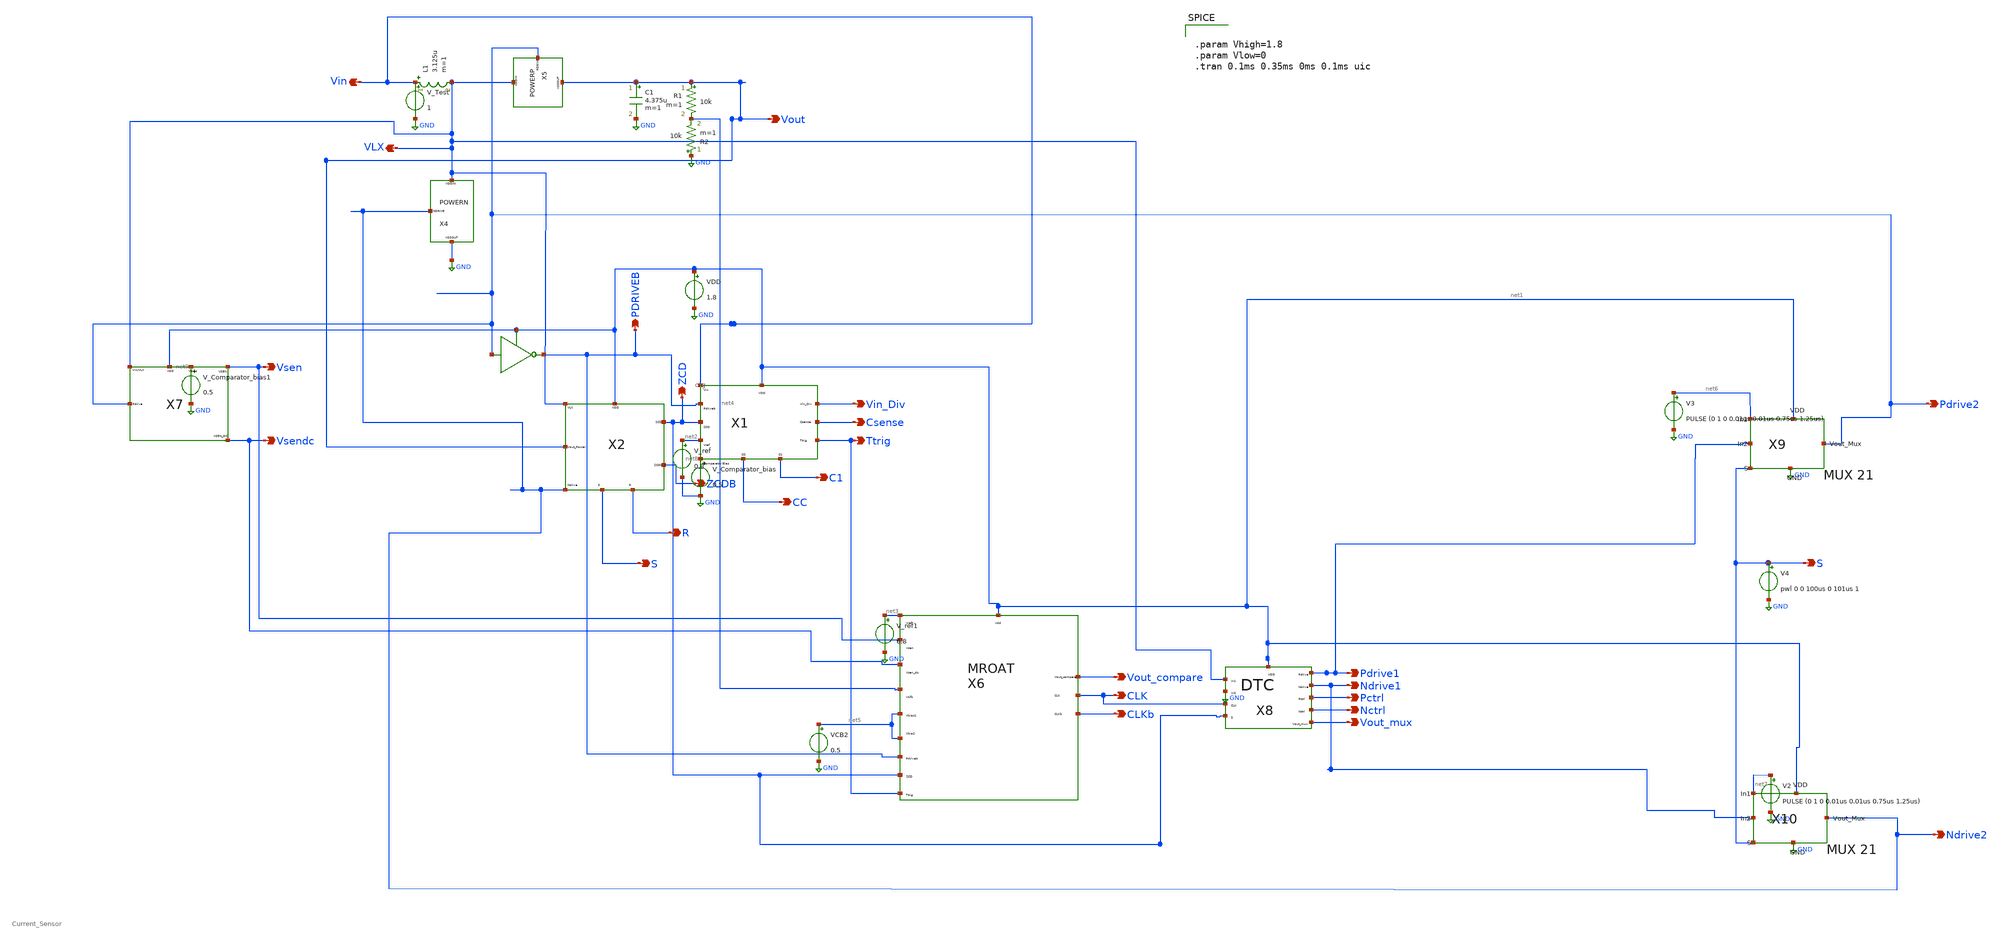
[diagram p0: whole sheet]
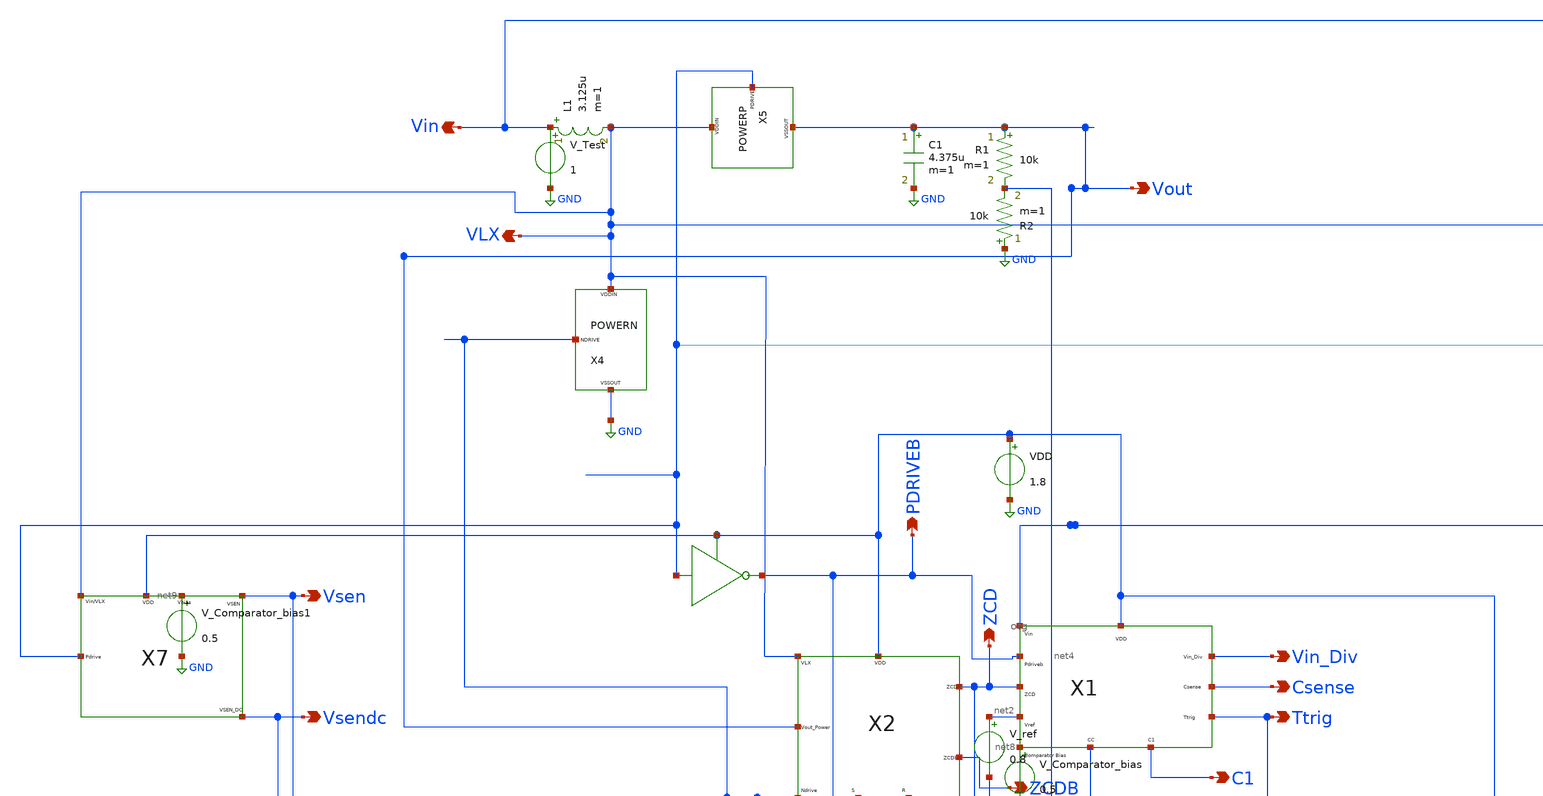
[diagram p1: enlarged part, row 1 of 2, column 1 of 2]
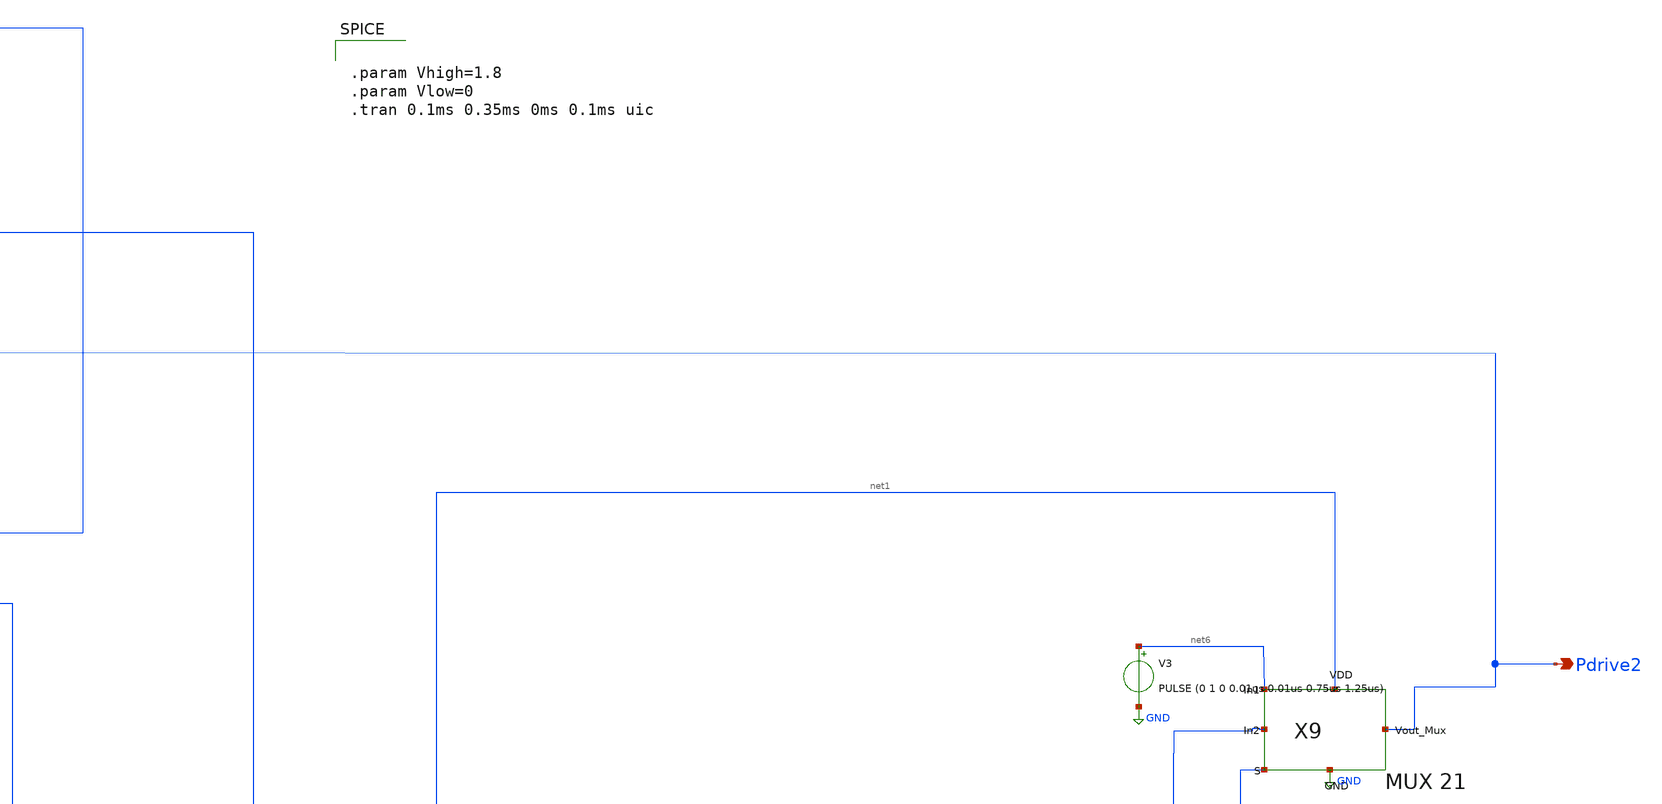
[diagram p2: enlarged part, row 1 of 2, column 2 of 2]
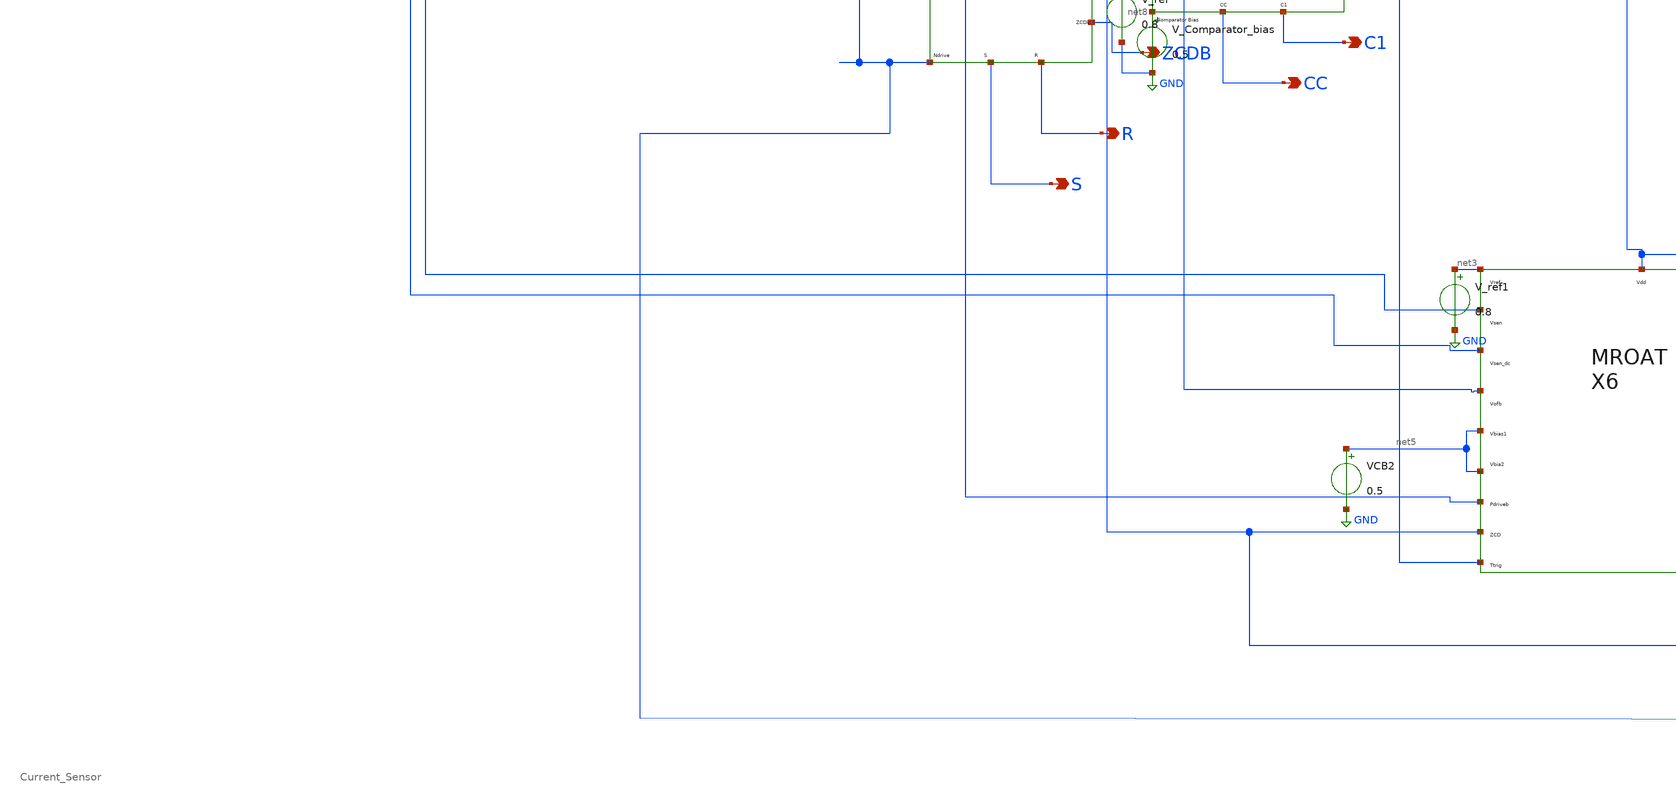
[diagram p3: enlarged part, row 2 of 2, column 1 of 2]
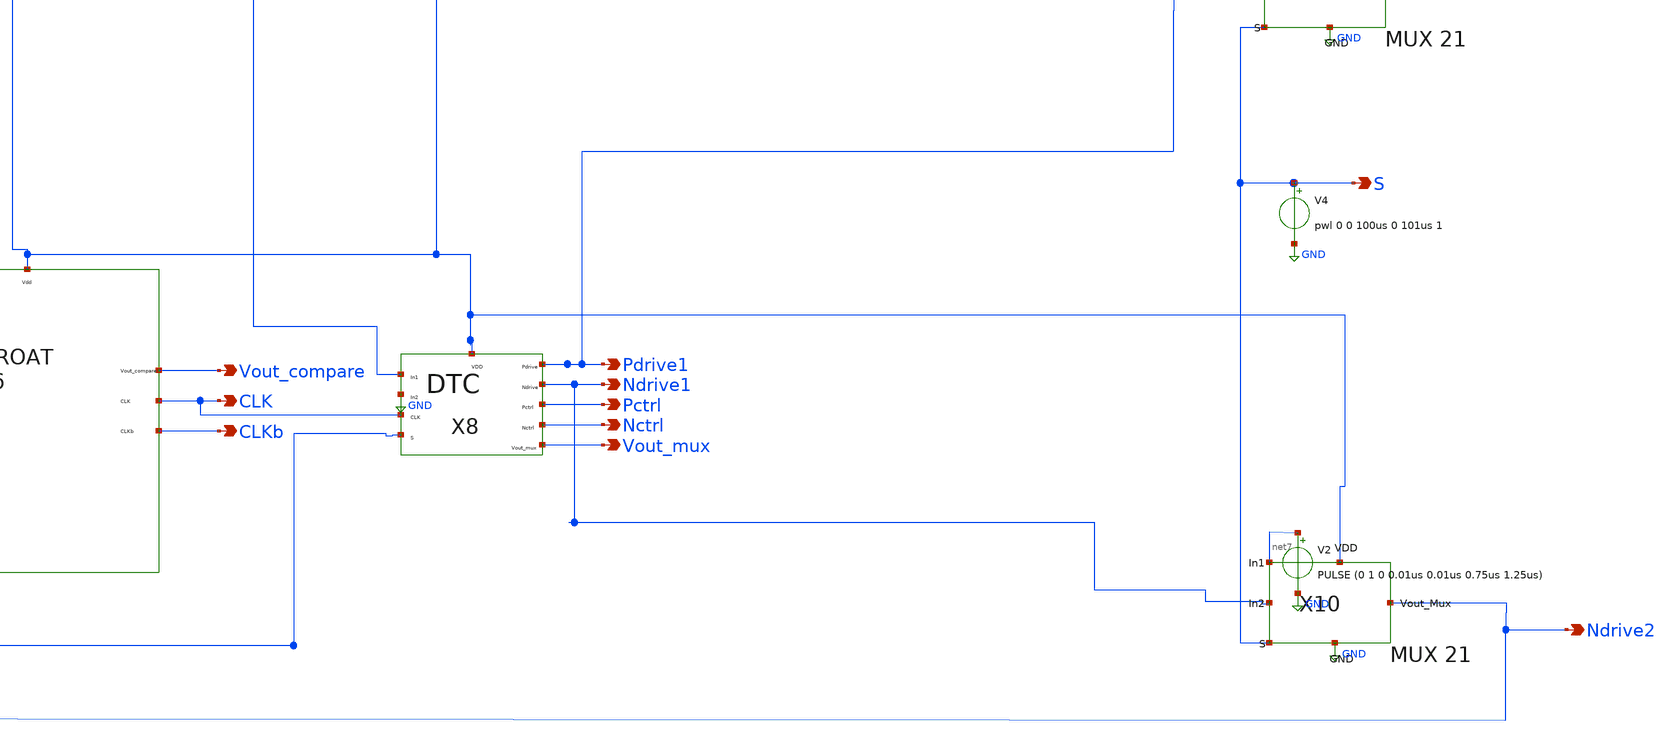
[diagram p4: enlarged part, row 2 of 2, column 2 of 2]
** sch_path: Current Sensor/fb_test.sch
**.subckt fb_test ZCD Vin_Div Csense Ttrig ZCDB PDRIVEB Vin VLX Vout C1 CC S R Vsen Vsendc
*+ Vout_compare CLK CLKb Pdrive1 Ndrive1 Pctrl Nctrl Vout_mux Pdrive2 Ndrive2 S
*.opin ZCD
*.opin Vin_Div
*.opin Csense
*.opin Ttrig
*.opin ZCDB
*.opin PDRIVEB
*.opin Vin
*.opin VLX
*.opin Vout
*.opin C1
*.opin CC
*.opin S
*.opin R
*.opin Vsen
*.opin Vsendc
*.opin Vout_compare
*.opin CLK
*.opin CLKb
*.opin Pdrive1
*.opin Ndrive1
*.opin Pctrl
*.opin Nctrl
*.opin Vout_mux
*.opin Pdrive2
*.opin Ndrive2
*.opin S
X1 Vin PDRIVEB ZCD net2 net8 net1 Vin_Div Csense Ttrig CC C1 otg
X2 VLX Vout Ndrive2 net1 ZCD ZCDB S R zcd
VDD net1 GND 1.8
V_Comparator_bias net8 GND 0.5
V_ref net2 GND 0.8
C1 Vout GND 4.375u m=1
R1 Vout net4 10k m=1
L1 Vin VLX 3.125u m=1
X4 Ndrive2 VLX GND powern
X5 Pdrive2 VLX Vout powerp
R2 GND net4 10k m=1
X7 Vsen Vsendc Pdrive2 VLX net1 net9 Current_Sensor
V_Comparator_bias1 net9 GND 0.5
X6 net3 Vsen Vsendc net4 net5 net5 net1 Vout_compare PDRIVEB ZCD Ttrig CLK CLKb mroat
V_ref1 net3 GND 0.8
VCB2 net5 GND 0.5
X8 net1 VLX GND CLK ZCD Pdrive1 Ndrive1 Pctrl Nctrl Vout_mux dtc
X9 net6 Pdrive1 S net1 Pdrive2 GND mux21
X10 net7 Ndrive1 S net1 Ndrive2 GND mux21
V3 net6 GND PULSE (0 1 0 0.01us 0.01us 0.75us 1.25us)
V2 net7 GND PULSE (0 1 0 0.01us 0.01us 0.75us 1.25us)
V4 S GND pwl 0 0 100us 0 101us 1
V_Test Vin GND 1
**** begin user architecture code

** opencircuitdesign pdks install
.lib $::SKYWATER_MODELS/sky130.lib.spice tt_mm




.param Vhigh=1.8
.param Vlow=0
.tran 0.1ms 0.35ms 0ms 0.1ms uic

**** end user architecture code
**.ends
.GLOBAL GND
.end
